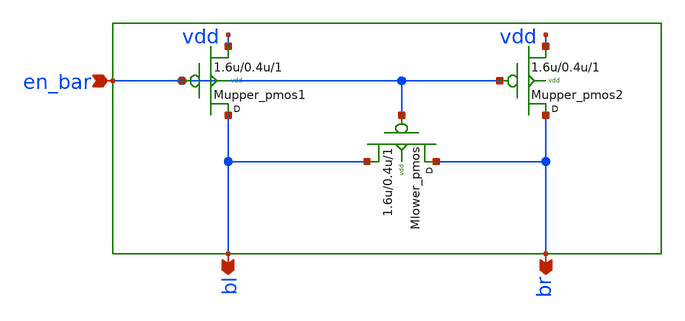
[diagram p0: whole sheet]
** sch_path: sram_2_64_scn4m_lcc/precharge_0.sch
**.subckt precharge_0 bl br en_bar
*.opin bl
*.opin br
*.ipin en_bar
Mupper_pmos1 bl en_bar vdd vdd p w=1.6u l=0.4u m=1
Mupper_pmos2 br en_bar vdd vdd p w=1.6u l=0.4u m=1
Mlower_pmos br en_bar bl vdd p w=1.6u l=0.4u m=1
**.ends
.end
